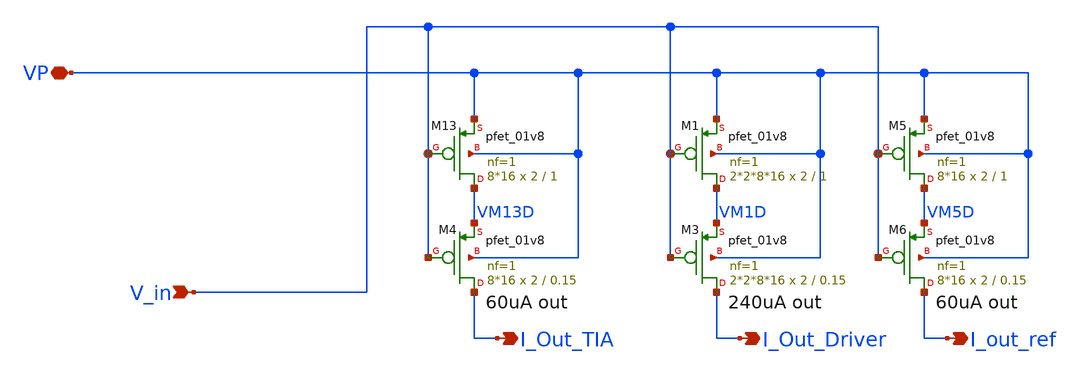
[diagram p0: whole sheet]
** sch_path: xschem/bias/current_mirror_channel_s.sch
**.subckt current_mirror_channel_s V_in VP I_Out_TIA I_Out_Driver I_out_ref
*.ipin V_in
*.iopin VP
*.opin I_Out_TIA
*.opin I_Out_Driver
*.opin I_out_ref
XM13 VM13D V_in VP VP sky130_fd_pr__pfet_01v8 L=1 W=2 nf=1 ad='int((nf+1)/2) * W/nf * 0.29' as='int((nf+2)/2) * W/nf * 0.29'
+ pd='2*int((nf+1)/2) * (W/nf + 0.29)' ps='2*int((nf+2)/2) * (W/nf + 0.29)' nrd='0.29 / W' nrs='0.29 / W'
+ sa=0 sb=0 sd=0 mult=8*16 m=8*16
XM4 I_Out_TIA V_in VM13D VP sky130_fd_pr__pfet_01v8 L=0.15 W=2 nf=1 ad='int((nf+1)/2) * W/nf * 0.29'
+ as='int((nf+2)/2) * W/nf * 0.29' pd='2*int((nf+1)/2) * (W/nf + 0.29)' ps='2*int((nf+2)/2) * (W/nf + 0.29)'
+ nrd='0.29 / W' nrs='0.29 / W' sa=0 sb=0 sd=0 mult=8*16 m=8*16
XM1 VM1D V_in VP VP sky130_fd_pr__pfet_01v8 L=1 W=2 nf=1 ad='int((nf+1)/2) * W/nf * 0.29' as='int((nf+2)/2) * W/nf * 0.29'
+ pd='2*int((nf+1)/2) * (W/nf + 0.29)' ps='2*int((nf+2)/2) * (W/nf + 0.29)' nrd='0.29 / W' nrs='0.29 / W'
+ sa=0 sb=0 sd=0 mult=2*2*8*16 m=2*2*8*16
XM3 I_Out_Driver V_in VM1D VP sky130_fd_pr__pfet_01v8 L=0.15 W=2 nf=1 ad='int((nf+1)/2) * W/nf * 0.29'
+ as='int((nf+2)/2) * W/nf * 0.29' pd='2*int((nf+1)/2) * (W/nf + 0.29)' ps='2*int((nf+2)/2) * (W/nf + 0.29)'
+ nrd='0.29 / W' nrs='0.29 / W' sa=0 sb=0 sd=0 mult=2*2*8*16 m=2*2*8*16
XM5 VM5D V_in VP VP sky130_fd_pr__pfet_01v8 L=1 W=2 nf=1 ad='int((nf+1)/2) * W/nf * 0.29' as='int((nf+2)/2) * W/nf * 0.29'
+ pd='2*int((nf+1)/2) * (W/nf + 0.29)' ps='2*int((nf+2)/2) * (W/nf + 0.29)' nrd='0.29 / W' nrs='0.29 / W'
+ sa=0 sb=0 sd=0 mult=8*16 m=8*16
XM6 I_out_ref V_in VM5D VP sky130_fd_pr__pfet_01v8 L=0.15 W=2 nf=1 ad='int((nf+1)/2) * W/nf * 0.29' as='int((nf+2)/2) * W/nf * 0.29'
+ pd='2*int((nf+1)/2) * (W/nf + 0.29)' ps='2*int((nf+2)/2) * (W/nf + 0.29)' nrd='0.29 / W' nrs='0.29 / W'
+ sa=0 sb=0 sd=0 mult=8*16 m=8*16
**.ends
.end
